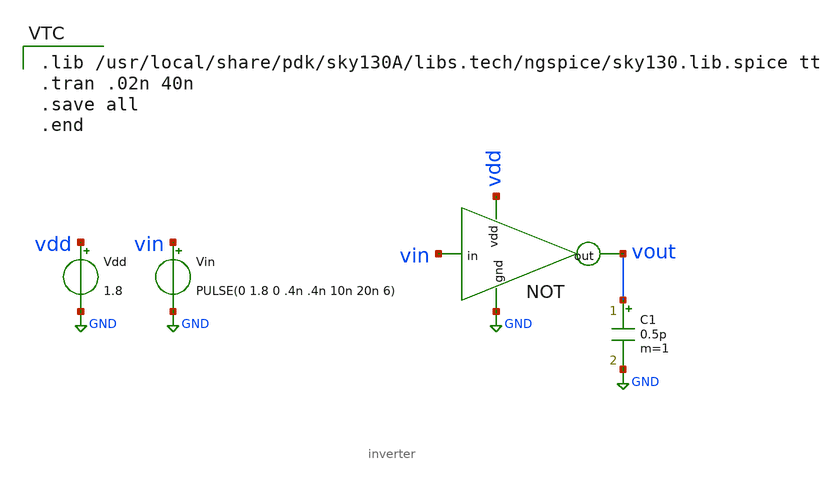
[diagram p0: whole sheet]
** sch_path: Projects/Design_and_Analysis_of_CMOS_Inverter:_Schematic_Design_Layout_Design_and_LVS_Validation_using_SKY130_PDK/assets/files/schematic_design/inv_testbench.sch
**.subckt inv_testbench
Vdd vdd GND 1.8
Vin vin GND PULSE(0 1.8 0 .4n .4n 10n 20n 6)
x1 vdd GND vin vout inverter
C1 vout GND 0.5p m=1
**** begin user architecture code

.lib /usr/local/share/pdk/sky130A/libs.tech/ngspice/sky130.lib.spice tt
.tran .02n 40n
.save all
.end

**** end user architecture code
**.ends

* expanding   symbol:  inverter.sym # of pins=4
** sym_path: Projects/Design_and_Analysis_of_CMOS_Inverter:_Schematic_Design_Layout_Design_and_LVS_Validation_using_SKY130_PDK/assets/files/schematic_design/inverter.sym
** sch_path: Projects/Design_and_Analysis_of_CMOS_Inverter:_Schematic_Design_Layout_Design_and_LVS_Validation_using_SKY130_PDK/assets/files/schematic_design/inverter.sch
.subckt inverter vdd gnd in out
*.ipin in
*.ipin vdd
*.ipin gnd
*.opin out
XM1 out in gnd gnd sky130_fd_pr__nfet_01v8 L=0.15 W=1 nf=1 ad='int((nf+1)/2) * W/nf * 0.29' as='int((nf+2)/2) * W/nf * 0.29'
+ pd='2*int((nf+1)/2) * (W/nf + 0.29)' ps='2*int((nf+2)/2) * (W/nf + 0.29)' nrd='0.29 / W' nrs='0.29 / W'
+ sa=0 sb=0 sd=0 mult=1 m=1
XM2 out in vdd vdd sky130_fd_pr__pfet_01v8 L=0.15 W=2 nf=1 ad='int((nf+1)/2) * W/nf * 0.29' as='int((nf+2)/2) * W/nf * 0.29'
+ pd='2*int((nf+1)/2) * (W/nf + 0.29)' ps='2*int((nf+2)/2) * (W/nf + 0.29)' nrd='0.29 / W' nrs='0.29 / W'
+ sa=0 sb=0 sd=0 mult=1 m=1
.ends

.GLOBAL GND
.end
